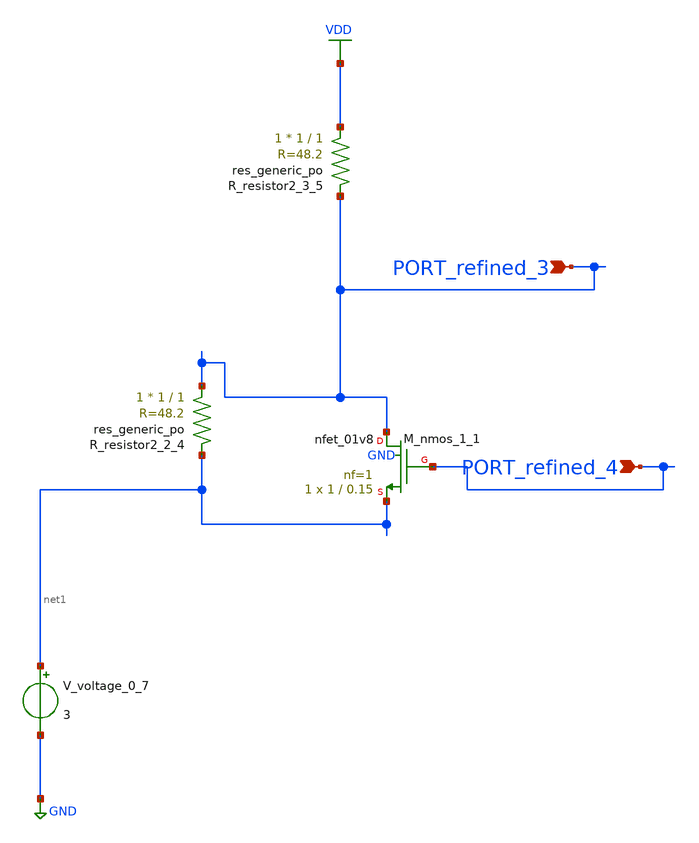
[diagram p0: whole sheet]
** sch_path: schematics/AMSNet/273.sch
**.subckt 273 PORT_refined_4 PORT_refined_3
*.ipin PORT_refined_4
*.ipin PORT_refined_3
XM_nmos_1_1 PORT_refined_3 PORT_refined_4 net1 GND sky130_fd_pr__nfet_01v8 L=0.15 W=1 nf=1 ad='int((1 + 1)/2) * 1 / 1 * 0.29'
+ as='int((1 + 2)/2) * 1 / 1 * 0.29' pd='2*int((1 + 1)/2) * (1 / 1 + 0.29)' ps='2*int((1 + 2)/2) * (1 / 1 + 0.29)'
+ nrd='0.29 / 1 ' nrs='0.29 / 1 ' sa=0 sb=0 sd=0 mult=1 m=1
XR_resistor2_2_4 PORT_refined_3 net1 sky130_fd_pr__res_generic_po W=1 L=1 m=1
XR_resistor2_3_5 VDD PORT_refined_3 sky130_fd_pr__res_generic_po W=1 L=1 m=1
V_voltage_0_7 net1 GND 3
**.ends
.GLOBAL GND
.GLOBAL VDD
.end
